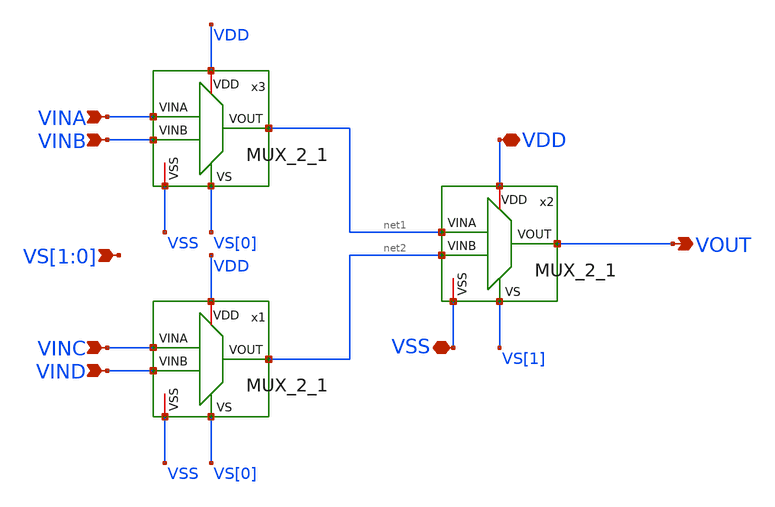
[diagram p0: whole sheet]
** sch_path: 27_03_26/TOP_MAXI/Esquematicos/MUX_4_1.sch
**.subckt MUX_4_1 VOUT VDD VSS VINA VINB VINC VIND VS[1],VS[0]
*.opin VOUT
*.iopin VDD
*.iopin VSS
*.ipin VINA
*.ipin VINB
*.ipin VINC
*.ipin VIND
*.ipin VS[1],VS[0]
x3 VDD VINA net1 VS[0] VINB VSS MUX_2_1
x1 VDD VINC net2 VS[0] VIND VSS MUX_2_1
x2 VDD net1 VOUT VS[1] net2 VSS MUX_2_1
**.ends
.end
